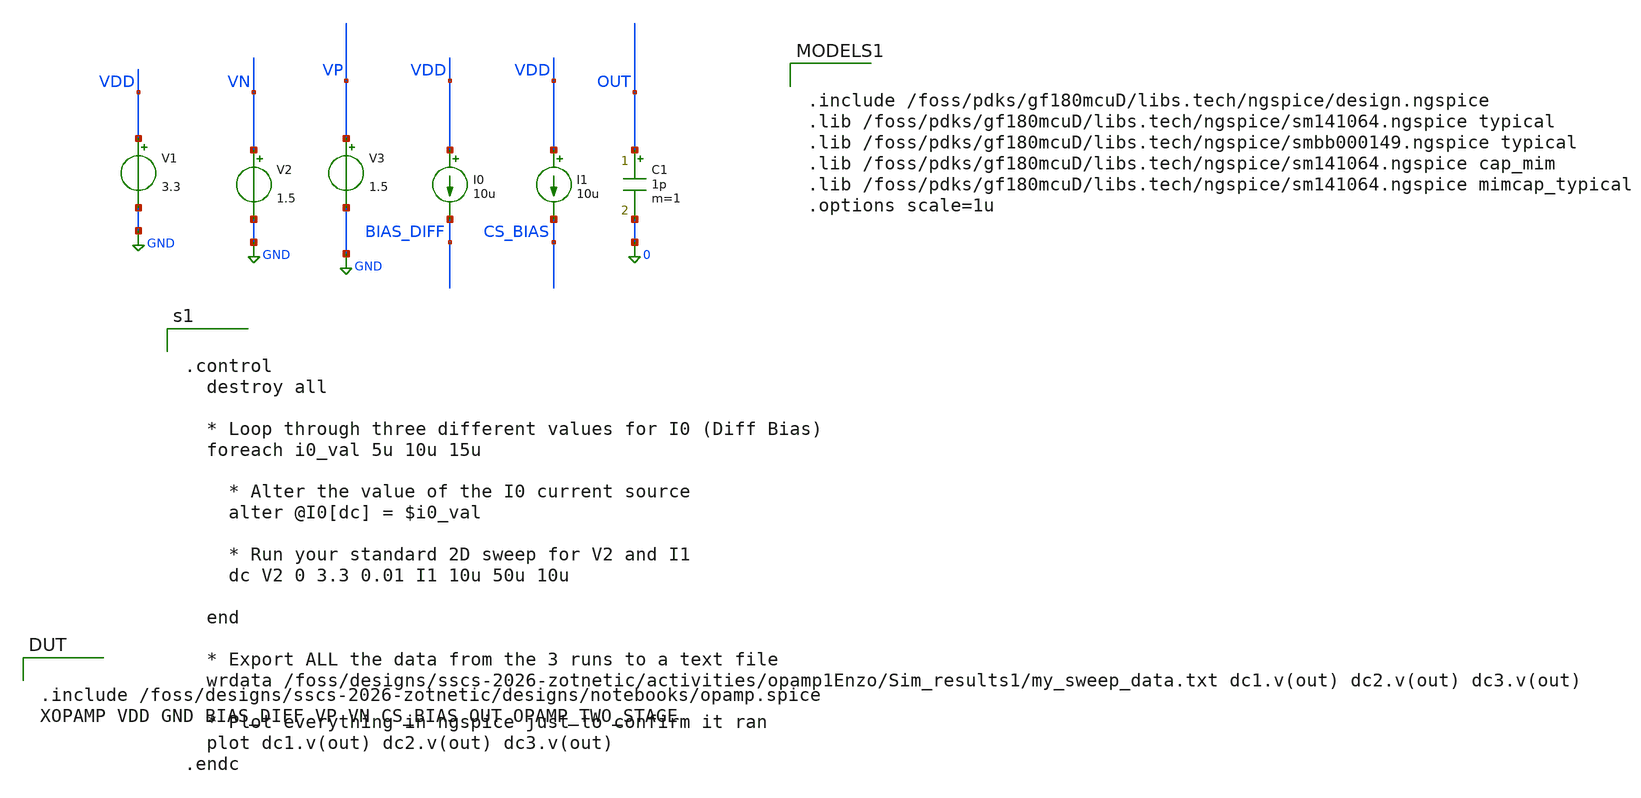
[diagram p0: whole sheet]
** sch_path: activities/opamp1Enzo/Act1T1.sch
**.subckt Act1T1
V1 VDD GND 3.3
V2 VN GND 1.5
C1 OUT 0 1p m=1
I0 VDD BIAS_DIFF 10u
I1 VDD CS_BIAS 10u
V3 VP GND 1.5
**** begin user architecture code


.control
  destroy all

  * Loop through three different values for I0 (Diff Bias)
  foreach i0_val 5u 10u 15u

    * Alter the value of the I0 current source
    alter @I0[dc] = $i0_val

    * Run your standard 2D sweep for V2 and I1
    dc V2 0 3.3 0.01 I1 10u 50u 10u

  end

  * Export ALL the data from the 3 runs to a text file
  wrdata /foss/designs/sscs-2026-zotnetic/activities/opamp1Enzo/Sim_results1/my_sweep_data.txt
+ dc1.v(out) dc2.v(out) dc3.v(out)

  * Plot everything in ngspice just to confirm it ran
  plot dc1.v(out) dc2.v(out) dc3.v(out)
.endc



.include /foss/pdks/gf180mcuD/libs.tech/ngspice/design.ngspice
.lib /foss/pdks/gf180mcuD/libs.tech/ngspice/sm141064.ngspice typical
.lib /foss/pdks/gf180mcuD/libs.tech/ngspice/smbb000149.ngspice typical
.lib /foss/pdks/gf180mcuD/libs.tech/ngspice/sm141064.ngspice cap_mim
.lib /foss/pdks/gf180mcuD/libs.tech/ngspice/sm141064.ngspice mimcap_typical
.options scale=1u



.include /foss/designs/sscs-2026-zotnetic/designs/notebooks/opamp.spice
XOPAMP VDD GND BIAS_DIFF VP VN CS_BIAS OUT OPAMP_TWO_STAGE
**** end user architecture code
**.ends
.GLOBAL GND
.end
